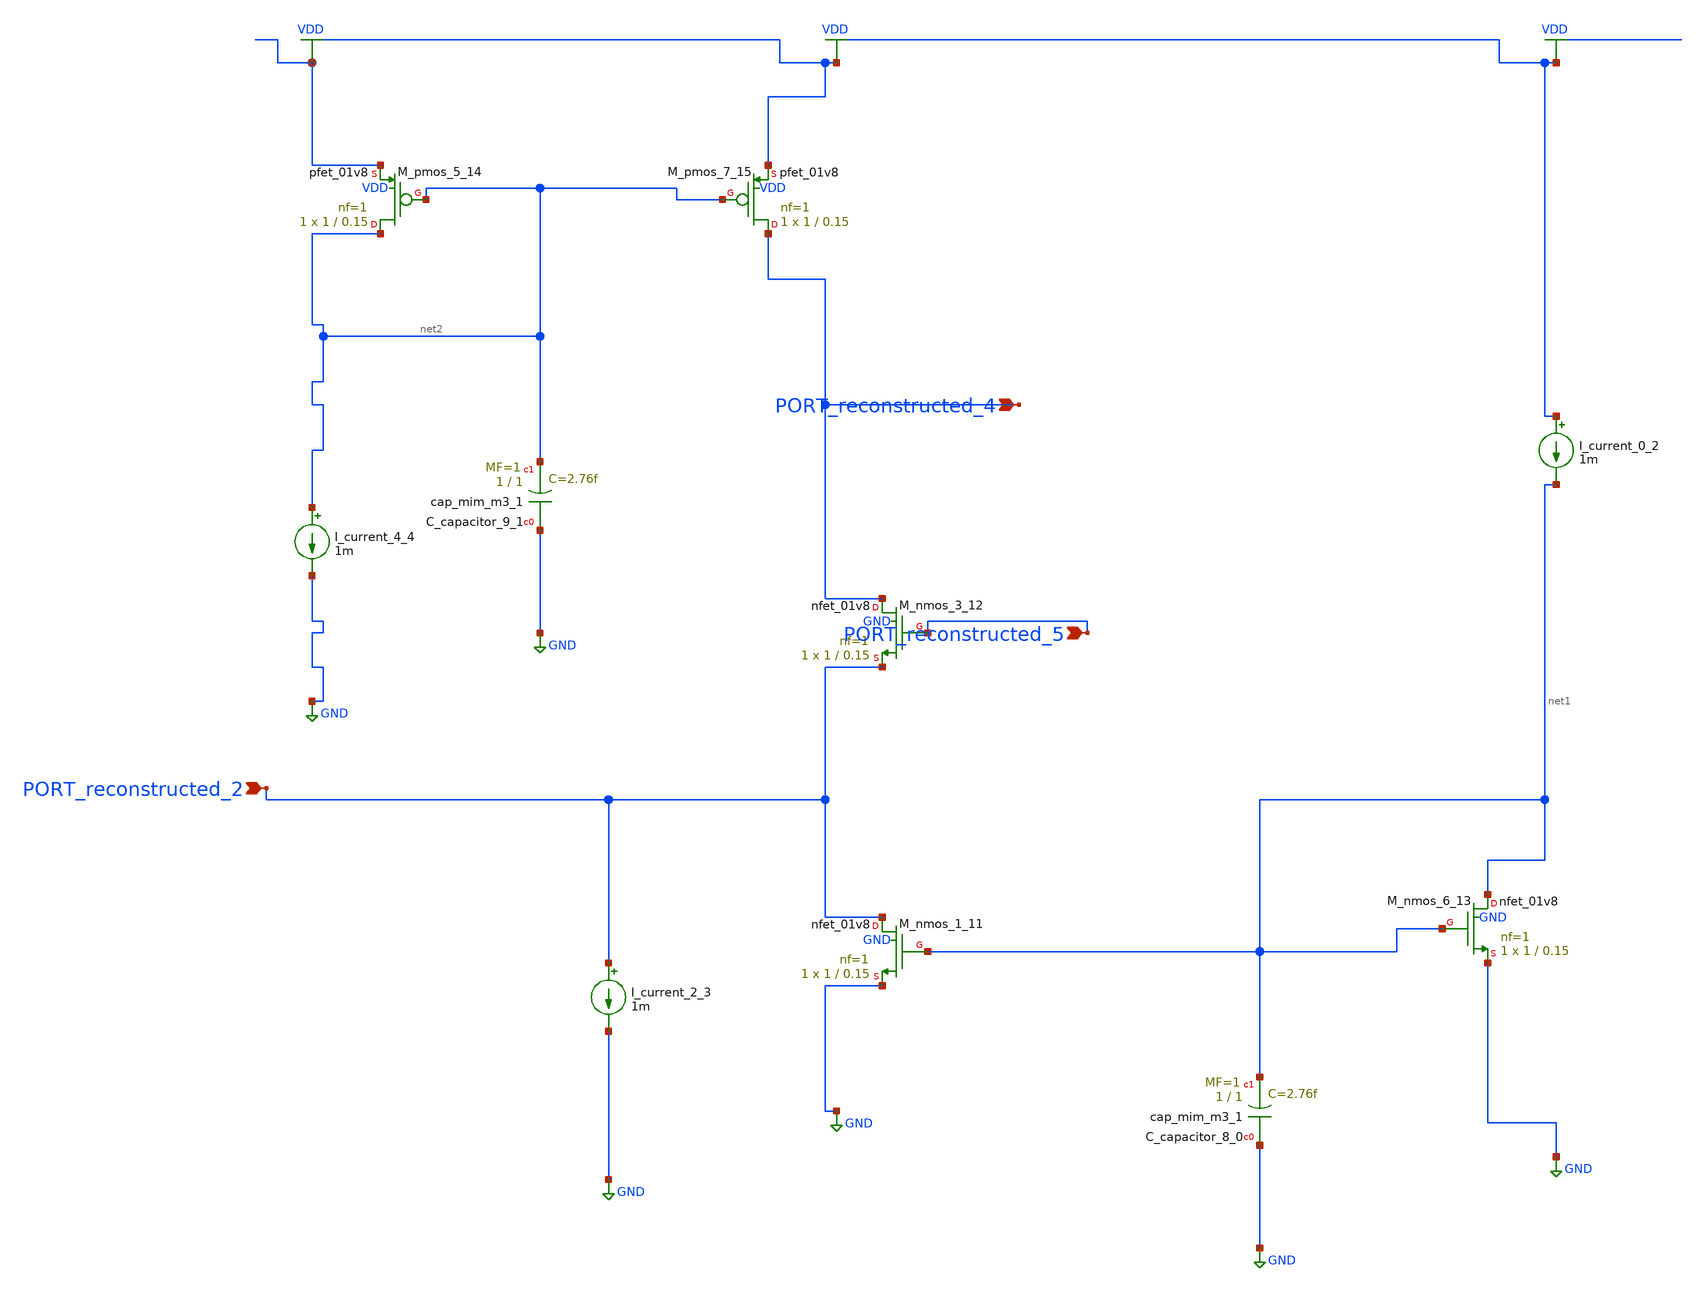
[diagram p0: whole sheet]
** sch_path: schematics/AMSNet/472.sch
**.subckt 472 PORT_reconstructed_4 PORT_reconstructed_5 PORT_reconstructed_2
*.ipin PORT_reconstructed_4
*.ipin PORT_reconstructed_5
*.ipin PORT_reconstructed_2
XC_capacitor_8_0 GND net1 sky130_fd_pr__cap_mim_m3_1 W=1 L=1 MF=1 m=1
XC_capacitor_9_1 GND net2 sky130_fd_pr__cap_mim_m3_1 W=1 L=1 MF=1 m=1
I_current_0_2 VDD net1 1m
I_current_2_3 PORT_reconstructed_2 GND 1m
I_current_4_4 net2 GND 1m
XM_nmos_1_11 PORT_reconstructed_2 net1 GND GND sky130_fd_pr__nfet_01v8 L=0.15 W=1 nf=1 ad='int((1 + 1)/2) * 1 / 1 * 0.29'
+ as='int((1 + 2)/2) * 1 / 1 * 0.29' pd='2*int((1 + 1)/2) * (1 / 1 + 0.29)' ps='2*int((1 + 2)/2) * (1 / 1 + 0.29)'
+ nrd='0.29 / 1 ' nrs='0.29 / 1 ' sa=0 sb=0 sd=0 mult=1 m=1
XM_nmos_3_12 PORT_reconstructed_4 PORT_reconstructed_5 PORT_reconstructed_2 GND sky130_fd_pr__nfet_01v8
+ L=0.15 W=1 nf=1 ad='int((1 + 1)/2) * 1 / 1 * 0.29' as='int((1 + 2)/2) * 1 / 1 * 0.29' pd='2*int((1 + 1)/2) * (1 / 1 + 0.29)'
+ ps='2*int((1 + 2)/2) * (1 / 1 + 0.29)' nrd='0.29 / 1 ' nrs='0.29 / 1 ' sa=0 sb=0 sd=0 mult=1 m=1
XM_nmos_6_13 net1 net1 GND GND sky130_fd_pr__nfet_01v8 L=0.15 W=1 nf=1 ad='int((1 + 1)/2) * 1 / 1 * 0.29'
+ as='int((1 + 2)/2) * 1 / 1 * 0.29' pd='2*int((1 + 1)/2) * (1 / 1 + 0.29)' ps='2*int((1 + 2)/2) * (1 / 1 + 0.29)'
+ nrd='0.29 / 1 ' nrs='0.29 / 1 ' sa=0 sb=0 sd=0 mult=1 m=1
XM_pmos_5_14 net2 net2 VDD VDD sky130_fd_pr__pfet_01v8 L=0.15 W=1 nf=1 ad='int((1 + 1)/2) * 1 / 1 * 0.29'
+ as='int((1 + 2)/2) * 1 / 1 * 0.29' pd='2*int((1 + 1)/2) * (1 / 1 + 0.29)' ps='2*int((1 + 2)/2) * (1 / 1 + 0.29)'
+ nrd='0.29 / 1 ' nrs='0.29 / 1 ' sa=0 sb=0 sd=0 mult=1 m=1
XM_pmos_7_15 PORT_reconstructed_4 net2 VDD VDD sky130_fd_pr__pfet_01v8 L=0.15 W=1 nf=1 ad='int((1 + 1)/2) * 1 / 1 * 0.29'
+ as='int((1 + 2)/2) * 1 / 1 * 0.29' pd='2*int((1 + 1)/2) * (1 / 1 + 0.29)' ps='2*int((1 + 2)/2) * (1 / 1 + 0.29)'
+ nrd='0.29 / 1 ' nrs='0.29 / 1 ' sa=0 sb=0 sd=0 mult=1 m=1
**.ends
.GLOBAL GND
.GLOBAL VDD
.end
